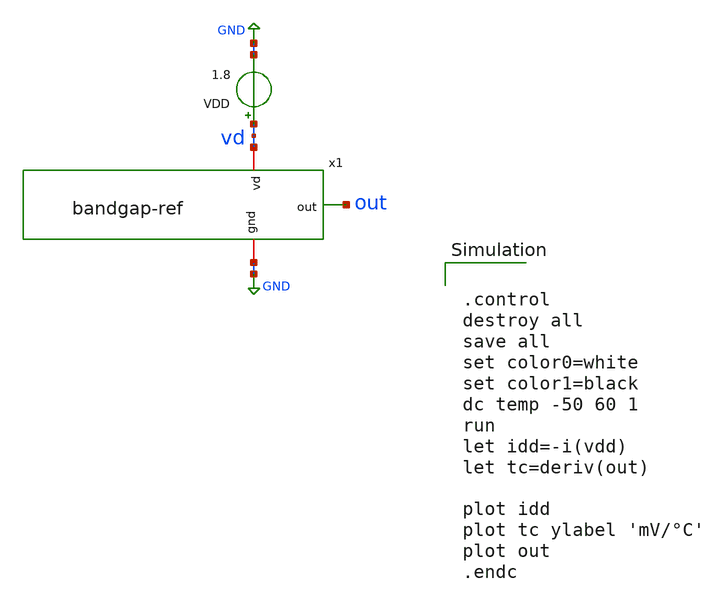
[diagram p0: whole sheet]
** sch_path: bandgap-ref/xschem/bandgap-ref_tb-temp.sch
**.subckt bandgap-ref_tb-temp
VDD vd GND 1.8
x1 vd out GND bandgap-ref
**** begin user architecture code


.control
destroy all
save all
set color0=white
set color1=black
dc temp -50 60 1
run
let idd=-i(vdd)
let tc=deriv(out)

plot idd
plot tc ylabel 'mV/°C'
plot out
.endc


 .lib $::SKYWATER_MODELS/sky130.lib.spice tt
.include $::SKYWATER_STDCELLS/sky130_fd_sc_hd.spice
.include /home/hugodg/sky130_workspace/skywater-pdk/libraries/sky130_fd_pr/latest/models/corners/tt/nonfet.spice
.include /home/hugodg/sky130_workspace/skywater-pdk/libraries/sky130_fd_pr/latest/cells/npn_05v5/sky130_fd_pr__npn_05v5__wafer.corner.spice

**** end user architecture code
**.ends

* expanding   symbol:  /home/hugodg/projects-sky130/temp-sensor/bandgap-ref/xschem/bandgap-ref.sym #
*+ of pins=3
** sym_path: bandgap-ref/xschem/bandgap-ref.sym
** sch_path: bandgap-ref/xschem/bandgap-ref.sch
.subckt bandgap-ref vd out gnd
*.iopin vd
*.iopin gnd
*.opin out
XP4 net4 vd net2 net2 sky130_fd_pr__pfet_01v8 L=2 W=30 nf=1 ad='int((nf+1)/2) * W/nf * 0.29' as='int((nf+2)/2) * W/nf * 0.29'
+ pd='2*int((nf+1)/2) * (W/nf + 0.29)' ps='2*int((nf+2)/2) * (W/nf + 0.29)' nrd='0.29 / W' nrs='0.29 / W'
+ sa=0 sb=0 sd=0 mult=1 m=1
XN1 net4 net4 net10 gnd sky130_fd_pr__nfet_01v8 L=2 W=10 nf=1 ad='int((nf+1)/2) * W/nf * 0.29' as='int((nf+2)/2) * W/nf * 0.29'
+ pd='2*int((nf+1)/2) * (W/nf + 0.29)' ps='2*int((nf+2)/2) * (W/nf + 0.29)' nrd='0.29 / W' nrs='0.29 / W'
+ sa=0 sb=0 sd=0 mult=1 m=1
XN2 net10 net10 net11 gnd sky130_fd_pr__nfet_01v8 L=2 W=10 nf=1 ad='int((nf+1)/2) * W/nf * 0.29' as='int((nf+2)/2) * W/nf * 0.29'
+ pd='2*int((nf+1)/2) * (W/nf + 0.29)' ps='2*int((nf+2)/2) * (W/nf + 0.29)' nrd='0.29 / W' nrs='0.29 / W'
+ sa=0 sb=0 sd=0 mult=1 m=1
XN3 net11 net11 gnd gnd sky130_fd_pr__nfet_01v8 L=2 W=10 nf=1 ad='int((nf+1)/2) * W/nf * 0.29' as='int((nf+2)/2) * W/nf * 0.29'
+ pd='2*int((nf+1)/2) * (W/nf + 0.29)' ps='2*int((nf+2)/2) * (W/nf + 0.29)' nrd='0.29 / W' nrs='0.29 / W'
+ sa=0 sb=0 sd=0 mult=1 m=1
XP5 net7 vd net1 net1 sky130_fd_pr__pfet_01v8 L=2 W=30 nf=1 ad='int((nf+1)/2) * W/nf * 0.29' as='int((nf+2)/2) * W/nf * 0.29'
+ pd='2*int((nf+1)/2) * (W/nf + 0.29)' ps='2*int((nf+2)/2) * (W/nf + 0.29)' nrd='0.29 / W' nrs='0.29 / W'
+ sa=0 sb=0 sd=0 mult=1 m=1
XP6 net8 vd vd vd sky130_fd_pr__pfet_01v8 L=2 W=30 nf=1 ad='int((nf+1)/2) * W/nf * 0.29' as='int((nf+2)/2) * W/nf * 0.29'
+ pd='2*int((nf+1)/2) * (W/nf + 0.29)' ps='2*int((nf+2)/2) * (W/nf + 0.29)' nrd='0.29 / W' nrs='0.29 / W'
+ sa=0 sb=0 sd=0 mult=1 m=1
XP7 net9 vd net3 net3 sky130_fd_pr__pfet_01v8 L=2 W=30 nf=1 ad='int((nf+1)/2) * W/nf * 0.29' as='int((nf+2)/2) * W/nf * 0.29'
+ pd='2*int((nf+1)/2) * (W/nf + 0.29)' ps='2*int((nf+2)/2) * (W/nf + 0.29)' nrd='0.29 / W' nrs='0.29 / W'
+ sa=0 sb=0 sd=0 mult=1 m=1
XP8 net6 net5 net7 net7 sky130_fd_pr__pfet_01v8 L=2 W=30 nf=1 ad='int((nf+1)/2) * W/nf * 0.29' as='int((nf+2)/2) * W/nf * 0.29'
+ pd='2*int((nf+1)/2) * (W/nf + 0.29)' ps='2*int((nf+2)/2) * (W/nf + 0.29)' nrd='0.29 / W' nrs='0.29 / W'
+ sa=0 sb=0 sd=0 mult=1 m=1
XP9 net6 net4 net5 net5 sky130_fd_pr__pfet_01v8 L=2 W=30 nf=1 ad='int((nf+1)/2) * W/nf * 0.29' as='int((nf+2)/2) * W/nf * 0.29'
+ pd='2*int((nf+1)/2) * (W/nf + 0.29)' ps='2*int((nf+2)/2) * (W/nf + 0.29)' nrd='0.29 / W' nrs='0.29 / W'
+ sa=0 sb=0 sd=0 mult=1 m=1
XP10 net5 net5 net8 net8 sky130_fd_pr__pfet_01v8 L=2 W=30 nf=1 ad='int((nf+1)/2) * W/nf * 0.29' as='int((nf+2)/2) * W/nf * 0.29'
+ pd='2*int((nf+1)/2) * (W/nf + 0.29)' ps='2*int((nf+2)/2) * (W/nf + 0.29)' nrd='0.29 / W' nrs='0.29 / W'
+ sa=0 sb=0 sd=0 mult=1 m=1
XP11 out net5 net9 net9 sky130_fd_pr__pfet_01v8 L=2 W=30 nf=1 ad='int((nf+1)/2) * W/nf * 0.29' as='int((nf+2)/2) * W/nf * 0.29'
+ pd='2*int((nf+1)/2) * (W/nf + 0.29)' ps='2*int((nf+2)/2) * (W/nf + 0.29)' nrd='0.29 / W' nrs='0.29 / W'
+ sa=0 sb=0 sd=0 mult=1 m=1
XN4 net6 net6 net12 gnd sky130_fd_pr__nfet_01v8 L=2 W=10 nf=1 ad='int((nf+1)/2) * W/nf * 0.29' as='int((nf+2)/2) * W/nf * 0.29'
+ pd='2*int((nf+1)/2) * (W/nf + 0.29)' ps='2*int((nf+2)/2) * (W/nf + 0.29)' nrd='0.29 / W' nrs='0.29 / W'
+ sa=0 sb=0 sd=0 mult=1 m=1
XN5 net12 net12 net15 gnd sky130_fd_pr__nfet_01v8 L=2 W=10 nf=1 ad='int((nf+1)/2) * W/nf * 0.29' as='int((nf+2)/2) * W/nf * 0.29'
+ pd='2*int((nf+1)/2) * (W/nf + 0.29)' ps='2*int((nf+2)/2) * (W/nf + 0.29)' nrd='0.29 / W' nrs='0.29 / W'
+ sa=0 sb=0 sd=0 mult=1 m=1
XN6 net5 net6 net13 gnd sky130_fd_pr__nfet_01v8 L=2 W=10 nf=1 ad='int((nf+1)/2) * W/nf * 0.29' as='int((nf+2)/2) * W/nf * 0.29'
+ pd='2*int((nf+1)/2) * (W/nf + 0.29)' ps='2*int((nf+2)/2) * (W/nf + 0.29)' nrd='0.29 / W' nrs='0.29 / W'
+ sa=0 sb=0 sd=0 mult=1 m=1
XN7 net13 net12 net14 gnd sky130_fd_pr__nfet_01v8 L=2 W=10 nf=1 ad='int((nf+1)/2) * W/nf * 0.29' as='int((nf+2)/2) * W/nf * 0.29'
+ pd='2*int((nf+1)/2) * (W/nf + 0.29)' ps='2*int((nf+2)/2) * (W/nf + 0.29)' nrd='0.29 / W' nrs='0.29 / W'
+ sa=0 sb=0 sd=0 mult=1 m=1
R1 net14 net16 1k m=1
R2 out net18 4.7k m=1
XD2 net15 gnd sky130_fd_pr__diode_pw2nd_05v5 area=1e12 pj=4e6
XQ1 net16 gnd gnd gnd sky130_fd_pr__npn_05v5_w1p00l2p00
XQ2 net16 gnd gnd gnd sky130_fd_pr__npn_05v5_w1p00l2p00
XQ3 net16 gnd gnd gnd sky130_fd_pr__npn_05v5_w1p00l2p00
XQ4 net16 gnd gnd gnd sky130_fd_pr__npn_05v5_w1p00l2p00
XQ5 net16 gnd gnd gnd sky130_fd_pr__npn_05v5_w1p00l2p00
XQ6 net16 gnd gnd gnd sky130_fd_pr__npn_05v5_w1p00l2p00
XQ7 net16 gnd gnd gnd sky130_fd_pr__npn_05v5_w1p00l2p00
XQ8 net16 gnd gnd gnd sky130_fd_pr__npn_05v5_w1p00l2p00
XQ9 net16 gnd gnd gnd sky130_fd_pr__npn_05v5_w1p00l2p00
XQ10 net18 gnd gnd gnd sky130_fd_pr__npn_05v5_w1p00l2p00
XQ11 net18 gnd gnd gnd sky130_fd_pr__npn_05v5_w1p00l2p00
XQ12 net18 gnd net17 net17 sky130_fd_pr__npn_05v5_w1p00l2p00
XQ13 net18 gnd net17 net17 sky130_fd_pr__npn_05v5_w1p00l2p00
XQ14 net18 gnd net17 net17 sky130_fd_pr__npn_05v5_w1p00l2p00
XQ15 net18 gnd net17 net17 sky130_fd_pr__npn_05v5_w1p00l2p00
XQ16 net18 gnd net17 net17 sky130_fd_pr__npn_05v5_w1p00l2p00
XQ17 net18 gnd net17 net17 sky130_fd_pr__npn_05v5_w1p00l2p00
XQ18 net18 gnd net17 net17 sky130_fd_pr__npn_05v5_w1p00l2p00
.ends

.GLOBAL GND
.end
